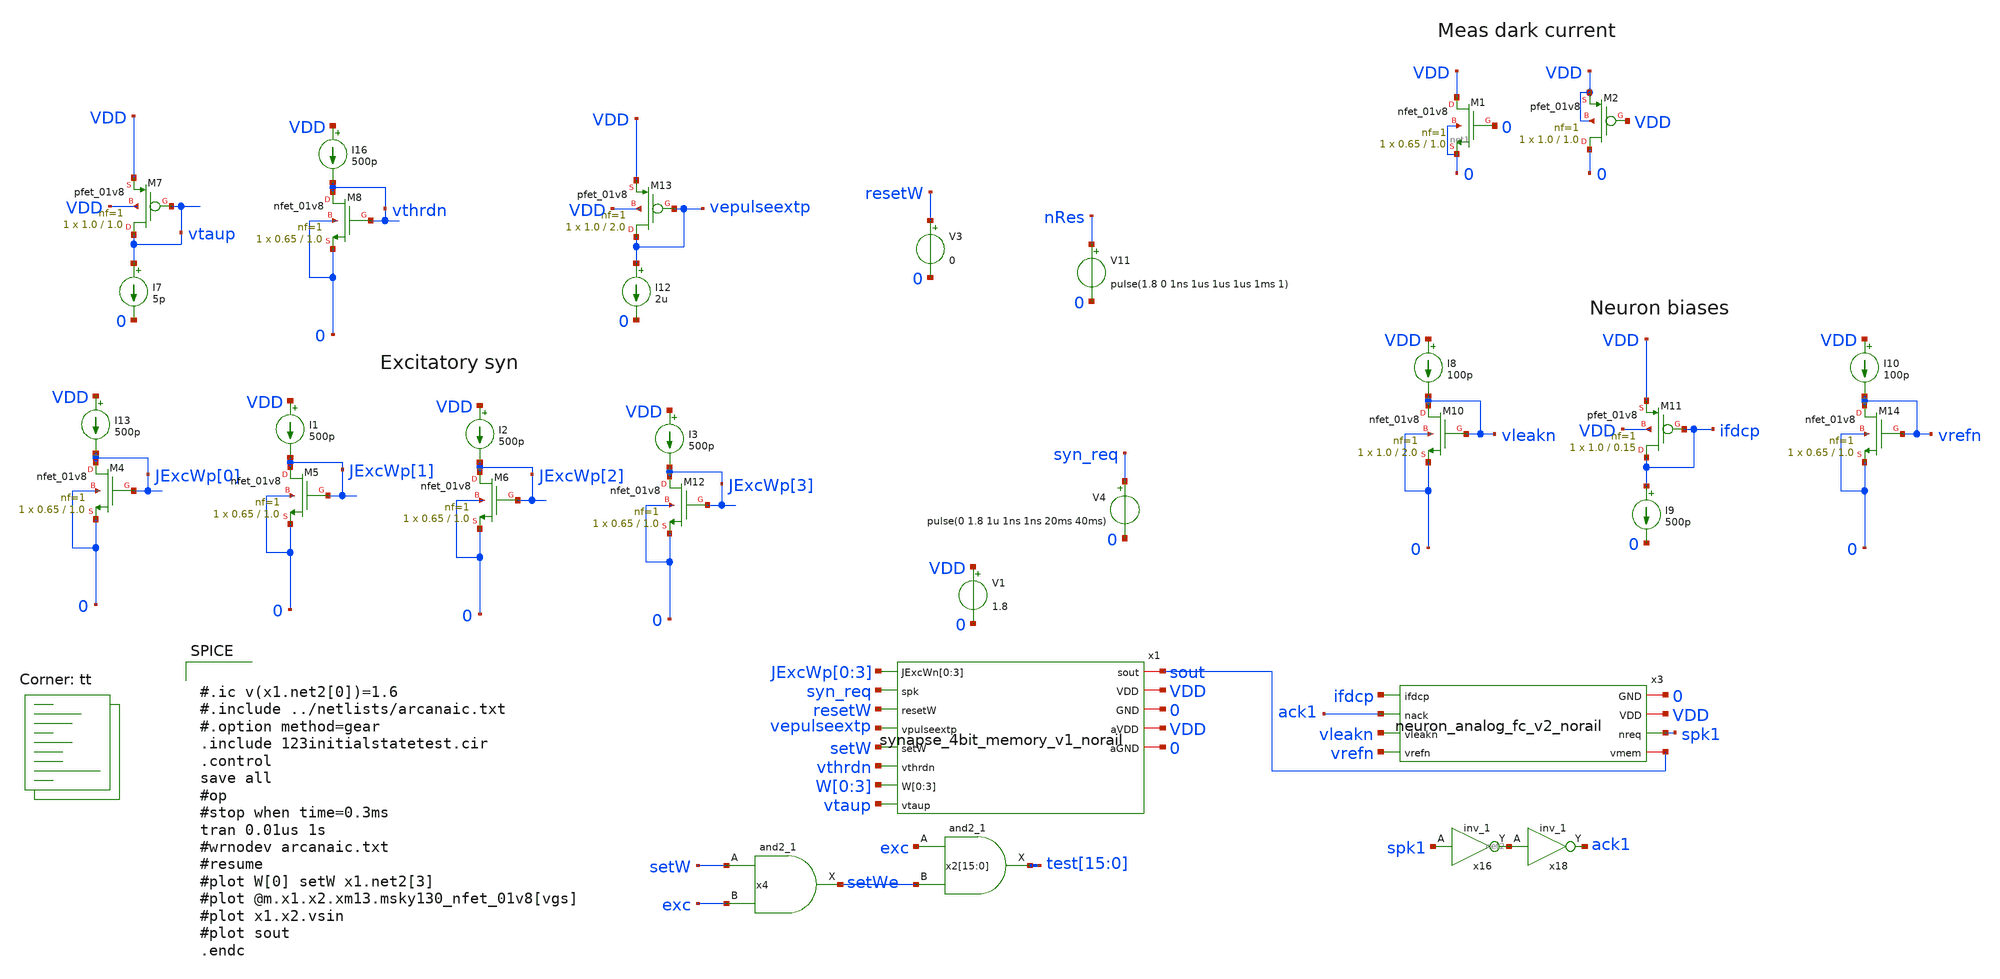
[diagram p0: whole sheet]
** sch_path: design/xschem/123initialstatetest.sch
**.subckt 123initialstatetest
x1 sout JExcWp[0] JExcWp[1] JExcWp[2] JExcWp[3] syn_req resetW vepulseextp setW vthrdn W[0] W[1]
+ W[2] W[3] vtaup VDD 0 VDD 0 synapse_4bit_memory_v1_norail
V1 VDD 0 1.8
XM7 vtaup vtaup VDD VDD sky130_fd_pr__pfet_01v8 L=1.0 W=1.0 nf=1 ad='int((nf+1)/2) * W/nf * 0.29' as='int((nf+2)/2) * W/nf * 0.29'
+ pd='2*int((nf+1)/2) * (W/nf + 0.29)' ps='2*int((nf+2)/2) * (W/nf + 0.29)' nrd='0.29 / W' nrs='0.29 / W'
+ sa=0 sb=0 sd=0 mult=1 m=1
I7 vtaup 0 5p
I16 VDD vthrdn 500p
XM8 vthrdn vthrdn 0 0 sky130_fd_pr__nfet_01v8 L=1.0 W=0.65 nf=1 ad='int((nf+1)/2) * W/nf * 0.29' as='int((nf+2)/2) * W/nf * 0.29'
+ pd='2*int((nf+1)/2) * (W/nf + 0.29)' ps='2*int((nf+2)/2) * (W/nf + 0.29)' nrd='0.29 / W' nrs='0.29 / W'
+ sa=0 sb=0 sd=0 mult=1 m=1
XM13 vepulseextp vepulseextp VDD VDD sky130_fd_pr__pfet_01v8 L=2.0 W=1.0 nf=1 ad='int((nf+1)/2) * W/nf * 0.29'
+ as='int((nf+2)/2) * W/nf * 0.29' pd='2*int((nf+1)/2) * (W/nf + 0.29)' ps='2*int((nf+2)/2) * (W/nf + 0.29)'
+ nrd='0.29 / W' nrs='0.29 / W' sa=0 sb=0 sd=0 mult=1 m=1
I12 vepulseextp 0 2u
V3 resetW 0 0
V11 nRes 0 pulse(1.8 0 1ns 1us 1us 1us 1ms 1)
x4 setW exc GND GND VDD VDD setWe sky130_fd_sc_hd__and2_1
x2[15] exc setWe GND GND VDD VDD test[15] sky130_fd_sc_hd__and2_1
x2[14] exc setWe GND GND VDD VDD test[14] sky130_fd_sc_hd__and2_1
x2[13] exc setWe GND GND VDD VDD test[13] sky130_fd_sc_hd__and2_1
x2[12] exc setWe GND GND VDD VDD test[12] sky130_fd_sc_hd__and2_1
x2[11] exc setWe GND GND VDD VDD test[11] sky130_fd_sc_hd__and2_1
x2[10] exc setWe GND GND VDD VDD test[10] sky130_fd_sc_hd__and2_1
x2[9] exc setWe GND GND VDD VDD test[9] sky130_fd_sc_hd__and2_1
x2[8] exc setWe GND GND VDD VDD test[8] sky130_fd_sc_hd__and2_1
x2[7] exc setWe GND GND VDD VDD test[7] sky130_fd_sc_hd__and2_1
x2[6] exc setWe GND GND VDD VDD test[6] sky130_fd_sc_hd__and2_1
x2[5] exc setWe GND GND VDD VDD test[5] sky130_fd_sc_hd__and2_1
x2[4] exc setWe GND GND VDD VDD test[4] sky130_fd_sc_hd__and2_1
x2[3] exc setWe GND GND VDD VDD test[3] sky130_fd_sc_hd__and2_1
x2[2] exc setWe GND GND VDD VDD test[2] sky130_fd_sc_hd__and2_1
x2[1] exc setWe GND GND VDD VDD test[1] sky130_fd_sc_hd__and2_1
x2[0] exc setWe GND GND VDD VDD test[0] sky130_fd_sc_hd__and2_1
V4 syn_req 0 pulse(0 1.8 1u 1ns 1ns 20ms 40ms)
XM1 VDD 0 0 net1 sky130_fd_pr__nfet_01v8 L=1.0 W=0.65 nf=1 ad='int((nf+1)/2) * W/nf * 0.29' as='int((nf+2)/2) * W/nf * 0.29'
+ pd='2*int((nf+1)/2) * (W/nf + 0.29)' ps='2*int((nf+2)/2) * (W/nf + 0.29)' nrd='0.29 / W' nrs='0.29 / W'
+ sa=0 sb=0 sd=0 mult=1 m=1
XM2 0 VDD VDD VDD sky130_fd_pr__pfet_01v8 L=1.0 W=1.0 nf=1 ad='int((nf+1)/2) * W/nf * 0.29' as='int((nf+2)/2) * W/nf * 0.29'
+ pd='2*int((nf+1)/2) * (W/nf + 0.29)' ps='2*int((nf+2)/2) * (W/nf + 0.29)' nrd='0.29 / W' nrs='0.29 / W'
+ sa=0 sb=0 sd=0 mult=1 m=1
x3 0 VDD spk1 ifdcp ack1 sout vleakn vrefn neuron_analog_fc_v2_norail
x16 spk1 0 0 VDD VDD net2 sky130_fd_sc_hd__inv_1
x18 net2 0 0 VDD VDD ack1 sky130_fd_sc_hd__inv_1
I8 VDD vleakn 100p
XM10 vleakn vleakn 0 0 sky130_fd_pr__nfet_01v8 L=2.0 W=1.0 nf=1 ad='int((nf+1)/2) * W/nf * 0.29' as='int((nf+2)/2) * W/nf * 0.29'
+ pd='2*int((nf+1)/2) * (W/nf + 0.29)' ps='2*int((nf+2)/2) * (W/nf + 0.29)' nrd='0.29 / W' nrs='0.29 / W'
+ sa=0 sb=0 sd=0 mult=1 m=1
XM11 ifdcp ifdcp VDD VDD sky130_fd_pr__pfet_01v8 L=0.15 W=1.0 nf=1 ad='int((nf+1)/2) * W/nf * 0.29' as='int((nf+2)/2) * W/nf * 0.29'
+ pd='2*int((nf+1)/2) * (W/nf + 0.29)' ps='2*int((nf+2)/2) * (W/nf + 0.29)' nrd='0.29 / W' nrs='0.29 / W'
+ sa=0 sb=0 sd=0 mult=1 m=1
I9 ifdcp 0 500p
I10 VDD vrefn 100p
XM14 vrefn vrefn 0 0 sky130_fd_pr__nfet_01v8 L=1.0 W=0.65 nf=1 ad='int((nf+1)/2) * W/nf * 0.29' as='int((nf+2)/2) * W/nf * 0.29'
+ pd='2*int((nf+1)/2) * (W/nf + 0.29)' ps='2*int((nf+2)/2) * (W/nf + 0.29)' nrd='0.29 / W' nrs='0.29 / W'
+ sa=0 sb=0 sd=0 mult=1 m=1
I13 VDD JExcWp[0] 500p
XM4 JExcWp[0] JExcWp[0] 0 0 sky130_fd_pr__nfet_01v8 L=1.0 W=0.65 nf=1 ad='int((nf+1)/2) * W/nf * 0.29'
+ as='int((nf+2)/2) * W/nf * 0.29' pd='2*int((nf+1)/2) * (W/nf + 0.29)' ps='2*int((nf+2)/2) * (W/nf + 0.29)'
+ nrd='0.29 / W' nrs='0.29 / W' sa=0 sb=0 sd=0 mult=1 m=1
I1 VDD JExcWp[1] 500p
XM5 JExcWp[1] JExcWp[1] 0 0 sky130_fd_pr__nfet_01v8 L=1.0 W=0.65 nf=1 ad='int((nf+1)/2) * W/nf * 0.29'
+ as='int((nf+2)/2) * W/nf * 0.29' pd='2*int((nf+1)/2) * (W/nf + 0.29)' ps='2*int((nf+2)/2) * (W/nf + 0.29)'
+ nrd='0.29 / W' nrs='0.29 / W' sa=0 sb=0 sd=0 mult=1 m=1
I2 VDD JExcWp[2] 500p
XM6 JExcWp[2] JExcWp[2] 0 0 sky130_fd_pr__nfet_01v8 L=1.0 W=0.65 nf=1 ad='int((nf+1)/2) * W/nf * 0.29'
+ as='int((nf+2)/2) * W/nf * 0.29' pd='2*int((nf+1)/2) * (W/nf + 0.29)' ps='2*int((nf+2)/2) * (W/nf + 0.29)'
+ nrd='0.29 / W' nrs='0.29 / W' sa=0 sb=0 sd=0 mult=1 m=1
I3 VDD JExcWp[3] 500p
XM12 JExcWp[3] JExcWp[3] 0 0 sky130_fd_pr__nfet_01v8 L=1.0 W=0.65 nf=1 ad='int((nf+1)/2) * W/nf * 0.29'
+ as='int((nf+2)/2) * W/nf * 0.29' pd='2*int((nf+1)/2) * (W/nf + 0.29)' ps='2*int((nf+2)/2) * (W/nf + 0.29)'
+ nrd='0.29 / W' nrs='0.29 / W' sa=0 sb=0 sd=0 mult=1 m=1
**** begin user architecture code
.lib $::SKYWATER_MODELS/sky130.lib.spice tt


#.ic v(x1.net2[0])=1.6
#.include ../netlists/arcanaic.txt
#.option method=gear
.include 123initialstatetest.cir
.control
save all
#op
#stop when time=0.3ms
tran 0.01us 1s
#wrnodev arcanaic.txt
#resume
#plot W[0] setW x1.net2[3]
#plot @m.x1.x2.xm13.msky130_nfet_01v8[vgs]
#plot x1.x2.vsin
#plot sout
.endc




* Standard cell simulation files
.include $::SKYWATER_STDCELLS/sky130_fd_sc_hd.spice


**** end user architecture code
**.ends

* expanding   symbol:  synapse_4bit_memory_v1_norail.sym # of pins=13
** sym_path: design/xschem/synapse_4bit_memory_v1_norail.sym
** sch_path: design/xschem/synapse_4bit_memory_v1_norail.sch
.subckt synapse_4bit_memory_v1_norail sout JExcWn[0] JExcWn[1] JExcWn[2] JExcWn[3] spk resetW
+ vpulseextp setW vthrdn W[0] W[1] W[2] W[3] vtaup VDD GND aVDD aGND
*.iopin GND
*.iopin VDD
*.ipin vpulseextp
*.ipin spk
*.ipin setW
*.ipin resetW
*.iopin sout
*.ipin vthrdn
*.ipin vtaup
*.iopin aVDD
*.ipin JExcWn[0],JExcWn[1],JExcWn[2],JExcWn[3]
*.ipin W[0],W[1],W[2],W[3]
*.iopin aGND
x2[0] setW W[0] net1 GND GND VDD VDD net2[3] sky130_fd_sc_hd__dfrtp_1
x2[1] setW W[1] net1 GND GND VDD VDD net2[2] sky130_fd_sc_hd__dfrtp_1
x2[2] setW W[2] net1 GND GND VDD VDD net2[1] sky130_fd_sc_hd__dfrtp_1
x2[3] setW W[3] net1 GND GND VDD VDD net2[0] sky130_fd_sc_hd__dfrtp_1
x4 resetW GND GND VDD VDD net1 sky130_fd_sc_hd__inv_1
x2 vtaup sout vthrdn spke JExcWn[0] JExcWn[1] JExcWn[2] JExcWn[3] aGND aVDD net2[3] net2[2] net2[1]
+ net2[0] dpi_syn_exc_4bit_fc_v2
x6 vpulseextp spk GND spke VDD spike_extender_with_trimming
x1 GND GND VDD VDD sky130_fd_sc_hd__decap_4
x3 GND GND VDD VDD sky130_fd_sc_hd__decap_3
x5 GND GND VDD VDD sky130_fd_sc_hd__decap_3
x7 GND GND VDD VDD sky130_fd_sc_hd__decap_6
x8 GND GND VDD VDD sky130_fd_sc_hd__decap_3
x9 GND GND VDD VDD sky130_fd_sc_hd__decap_3
.ends


* expanding   symbol:  neuron_analog_fc_v2_norail.sym # of pins=8
** sym_path: design/xschem/neuron_analog_fc_v2_norail.sym
** sch_path: design/xschem/neuron_analog_fc_v2_norail.sch
.subckt neuron_analog_fc_v2_norail GND VDD nreq ifdcp nack vmem vleakn vrefn
*.ipin vleakn
*.iopin GND
*.iopin VDD
*.opin nreq
*.ipin vrefn
*.ipin nack
*.ipin ifdcp
*.iopin vmem
XC1 GND vmem sky130_fd_pr__cap_mim_m3_1 W=5 L=5 MF=1 m=1
XM1 vmem ifdcp VDD VDD sky130_fd_pr__pfet_01v8 L=2.0 W=1.0 nf=1 ad='int((nf+1)/2) * W/nf * 0.29' as='int((nf+2)/2) * W/nf * 0.29'
+ pd='2*int((nf+1)/2) * (W/nf + 0.29)' ps='2*int((nf+2)/2) * (W/nf + 0.29)' nrd='0.29 / W' nrs='0.29 / W'
+ sa=0 sb=0 sd=0 mult=1 m=1
XM5 net2 nreq VDD VDD sky130_fd_pr__pfet_01v8 L=0.25 W=1.0 nf=1 ad='int((nf+1)/2) * W/nf * 0.29' as='int((nf+2)/2) * W/nf * 0.29'
+ pd='2*int((nf+1)/2) * (W/nf + 0.29)' ps='2*int((nf+2)/2) * (W/nf + 0.29)' nrd='0.29 / W' nrs='0.29 / W'
+ sa=0 sb=0 sd=0 mult=1 m=1
XM7 net3 nreq net4 GND sky130_fd_pr__nfet_01v8 L=0.15 W=0.6 nf=1 ad='int((nf+1)/2) * W/nf * 0.29' as='int((nf+2)/2) * W/nf * 0.29'
+ pd='2*int((nf+1)/2) * (W/nf + 0.29)' ps='2*int((nf+2)/2) * (W/nf + 0.29)' nrd='0.29 / W' nrs='0.29 / W'
+ sa=0 sb=0 sd=0 mult=1 m=1
XM6 net5 nack VDD VDD sky130_fd_pr__pfet_01v8 L=0.25 W=1.0 nf=1 ad='int((nf+1)/2) * W/nf * 0.29' as='int((nf+2)/2) * W/nf * 0.29'
+ pd='2*int((nf+1)/2) * (W/nf + 0.29)' ps='2*int((nf+2)/2) * (W/nf + 0.29)' nrd='0.29 / W' nrs='0.29 / W'
+ sa=0 sb=0 sd=0 mult=1 m=1
XM9 nreq vmem net2 VDD sky130_fd_pr__pfet_01v8 L=0.15 W=1.0 nf=1 ad='int((nf+1)/2) * W/nf * 0.29' as='int((nf+2)/2) * W/nf * 0.29'
+ pd='2*int((nf+1)/2) * (W/nf + 0.29)' ps='2*int((nf+2)/2) * (W/nf + 0.29)' nrd='0.29 / W' nrs='0.29 / W'
+ sa=0 sb=0 sd=0 mult=1 m=1
XM10 net3 nreq net5 VDD sky130_fd_pr__pfet_01v8 L=0.15 W=1.0 nf=1 ad='int((nf+1)/2) * W/nf * 0.29' as='int((nf+2)/2) * W/nf * 0.29'
+ pd='2*int((nf+1)/2) * (W/nf + 0.29)' ps='2*int((nf+2)/2) * (W/nf + 0.29)' nrd='0.29 / W' nrs='0.29 / W'
+ sa=0 sb=0 sd=0 mult=1 m=1
XM4 vmem nreq VDD VDD sky130_fd_pr__pfet_01v8 L=1.0 W=1.0 nf=1 ad='int((nf+1)/2) * W/nf * 0.29' as='int((nf+2)/2) * W/nf * 0.29'
+ pd='2*int((nf+1)/2) * (W/nf + 0.29)' ps='2*int((nf+2)/2) * (W/nf + 0.29)' nrd='0.29 / W' nrs='0.29 / W'
+ sa=0 sb=0 sd=0 mult=1 m=1
XM2 nreq vmem net1 GND sky130_fd_pr__nfet_01v8 L=0.15 W=0.6 nf=1 ad='int((nf+1)/2) * W/nf * 0.29' as='int((nf+2)/2) * W/nf * 0.29'
+ pd='2*int((nf+1)/2) * (W/nf + 0.29)' ps='2*int((nf+2)/2) * (W/nf + 0.29)' nrd='0.29 / W' nrs='0.29 / W'
+ sa=0 sb=0 sd=0 mult=1 m=1
XM3 net4 vrefn GND GND sky130_fd_pr__nfet_01v8 L=1.0 W=0.6 nf=1 ad='int((nf+1)/2) * W/nf * 0.29' as='int((nf+2)/2) * W/nf * 0.29'
+ pd='2*int((nf+1)/2) * (W/nf + 0.29)' ps='2*int((nf+2)/2) * (W/nf + 0.29)' nrd='0.29 / W' nrs='0.29 / W'
+ sa=0 sb=0 sd=0 mult=1 m=1
XM8 net1 net1 GND GND sky130_fd_pr__nfet_01v8 L=0.15 W=0.6 nf=1 ad='int((nf+1)/2) * W/nf * 0.29' as='int((nf+2)/2) * W/nf * 0.29'
+ pd='2*int((nf+1)/2) * (W/nf + 0.29)' ps='2*int((nf+2)/2) * (W/nf + 0.29)' nrd='0.29 / W' nrs='0.29 / W'
+ sa=0 sb=0 sd=0 mult=1 m=1
XM11 vmem net3 GND GND sky130_fd_pr__nfet_01v8 L=0.2 W=1.0 nf=1 ad='int((nf+1)/2) * W/nf * 0.29' as='int((nf+2)/2) * W/nf * 0.29'
+ pd='2*int((nf+1)/2) * (W/nf + 0.29)' ps='2*int((nf+2)/2) * (W/nf + 0.29)' nrd='0.29 / W' nrs='0.29 / W'
+ sa=0 sb=0 sd=0 mult=1 m=1
XM12 vmem vleakn GND GND sky130_fd_pr__nfet_01v8 L=2.0 W=1.0 nf=1 ad='int((nf+1)/2) * W/nf * 0.29' as='int((nf+2)/2) * W/nf * 0.29'
+ pd='2*int((nf+1)/2) * (W/nf + 0.29)' ps='2*int((nf+2)/2) * (W/nf + 0.29)' nrd='0.29 / W' nrs='0.29 / W'
+ sa=0 sb=0 sd=0 mult=1 m=1
XM13 GND net3 GND GND sky130_fd_pr__nfet_01v8 L=2.0 W=1.0 nf=1 ad='int((nf+1)/2) * W/nf * 0.29' as='int((nf+2)/2) * W/nf * 0.29'
+ pd='2*int((nf+1)/2) * (W/nf + 0.29)' ps='2*int((nf+2)/2) * (W/nf + 0.29)' nrd='0.29 / W' nrs='0.29 / W'
+ sa=0 sb=0 sd=0 mult=1 m=1
.ends


* expanding   symbol:  dpi_syn_exc_4bit_fc_v2.sym # of pins=8
** sym_path: design/xschem/dpi_syn_exc_4bit_fc_v2.sym
** sch_path: design/xschem/dpi_syn_exc_4bit_fc_v2.sch
.subckt dpi_syn_exc_4bit_fc_v2 vtaup sout vthn spk JExcWn[0] JExcWn[1] JExcWn[2] JExcWn[3] GND aVDD
+ weight[0] weight[1] weight[2] weight[3]
*.iopin GND
*.iopin aVDD
*.iopin vtaup
*.ipin spk
*.opin sout
*.iopin vthn
*.ipin weight[0],weight[1],weight[2],weight[3]
*.iopin JExcWn[0],JExcWn[1],JExcWn[2],JExcWn[3]
XM2 net3 spk net1 GND sky130_fd_pr__nfet_01v8 L=0.25 W=1.0 nf=1 ad='int((nf+1)/2) * W/nf * 0.29' as='int((nf+2)/2) * W/nf * 0.29'
+ pd='2*int((nf+1)/2) * (W/nf + 0.29)' ps='2*int((nf+2)/2) * (W/nf + 0.29)' nrd='0.29 / W' nrs='0.29 / W'
+ sa=0 sb=0 sd=0 mult=1 m=1
XC1 vsin aVDD sky130_fd_pr__cap_mim_m3_1 W=5 L=5 MF=1 m=1
XM5 vsin vtaup aVDD aVDD sky130_fd_pr__pfet_01v8 L=0.2 W=1.2 nf=1 ad='int((nf+1)/2) * W/nf * 0.29' as='int((nf+2)/2) * W/nf * 0.29'
+ pd='2*int((nf+1)/2) * (W/nf + 0.29)' ps='2*int((nf+2)/2) * (W/nf + 0.29)' nrd='0.29 / W' nrs='0.29 / W'
+ sa=0 sb=0 sd=0 mult=1 m=1
XM6 sout vsin aVDD aVDD sky130_fd_pr__pfet_01v8 L=0.2 W=1.2 nf=1 ad='int((nf+1)/2) * W/nf * 0.29' as='int((nf+2)/2) * W/nf * 0.29'
+ pd='2*int((nf+1)/2) * (W/nf + 0.29)' ps='2*int((nf+2)/2) * (W/nf + 0.29)' nrd='0.29 / W' nrs='0.29 / W'
+ sa=0 sb=0 sd=0 mult=1 m=1
XM1 net1 JExcWn[0] net2 GND sky130_fd_pr__nfet_01v8 L=1.0 W=1.0 nf=1 ad='int((nf+1)/2) * W/nf * 0.29'
+ as='int((nf+2)/2) * W/nf * 0.29' pd='2*int((nf+1)/2) * (W/nf + 0.29)' ps='2*int((nf+2)/2) * (W/nf + 0.29)'
+ nrd='0.29 / W' nrs='0.29 / W' sa=0 sb=0 sd=0 mult=1 m=1
XM4 vsin vsin net3 GND sky130_fd_pr__nfet_01v8 L=0.25 W=1.0 nf=1 ad='int((nf+1)/2) * W/nf * 0.29' as='int((nf+2)/2) * W/nf * 0.29'
+ pd='2*int((nf+1)/2) * (W/nf + 0.29)' ps='2*int((nf+2)/2) * (W/nf + 0.29)' nrd='0.29 / W' nrs='0.29 / W'
+ sa=0 sb=0 sd=0 mult=1 m=1
XM3 aVDD vthn net3 GND sky130_fd_pr__nfet_01v8 L=0.25 W=1.0 nf=1 ad='int((nf+1)/2) * W/nf * 0.29' as='int((nf+2)/2) * W/nf * 0.29'
+ pd='2*int((nf+1)/2) * (W/nf + 0.29)' ps='2*int((nf+2)/2) * (W/nf + 0.29)' nrd='0.29 / W' nrs='0.29 / W'
+ sa=0 sb=0 sd=0 mult=1 m=1
XM7 net1 JExcWn[1] net4 GND sky130_fd_pr__nfet_01v8 L=2.0 W=1.0 nf=1 ad='int((nf+1)/2) * W/nf * 0.29'
+ as='int((nf+2)/2) * W/nf * 0.29' pd='2*int((nf+1)/2) * (W/nf + 0.29)' ps='2*int((nf+2)/2) * (W/nf + 0.29)'
+ nrd='0.29 / W' nrs='0.29 / W' sa=0 sb=0 sd=0 mult=1 m=1
XM8 net1 JExcWn[2] net5 GND sky130_fd_pr__nfet_01v8 L=4.0 W=1.0 nf=1 ad='int((nf+1)/2) * W/nf * 0.29'
+ as='int((nf+2)/2) * W/nf * 0.29' pd='2*int((nf+1)/2) * (W/nf + 0.29)' ps='2*int((nf+2)/2) * (W/nf + 0.29)'
+ nrd='0.29 / W' nrs='0.29 / W' sa=0 sb=0 sd=0 mult=1 m=1
XM9 net1 JExcWn[3] net6 GND sky130_fd_pr__nfet_01v8 L=8.0 W=1.0 nf=1 ad='int((nf+1)/2) * W/nf * 0.29'
+ as='int((nf+2)/2) * W/nf * 0.29' pd='2*int((nf+1)/2) * (W/nf + 0.29)' ps='2*int((nf+2)/2) * (W/nf + 0.29)'
+ nrd='0.29 / W' nrs='0.29 / W' sa=0 sb=0 sd=0 mult=1 m=1
XM10 net2 weight[0] GND GND sky130_fd_pr__nfet_01v8 L=0.25 W=1.0 nf=1 ad='int((nf+1)/2) * W/nf * 0.29'
+ as='int((nf+2)/2) * W/nf * 0.29' pd='2*int((nf+1)/2) * (W/nf + 0.29)' ps='2*int((nf+2)/2) * (W/nf + 0.29)'
+ nrd='0.29 / W' nrs='0.29 / W' sa=0 sb=0 sd=0 mult=1 m=1
XM11 net4 weight[1] GND GND sky130_fd_pr__nfet_01v8 L=0.25 W=1.0 nf=1 ad='int((nf+1)/2) * W/nf * 0.29'
+ as='int((nf+2)/2) * W/nf * 0.29' pd='2*int((nf+1)/2) * (W/nf + 0.29)' ps='2*int((nf+2)/2) * (W/nf + 0.29)'
+ nrd='0.29 / W' nrs='0.29 / W' sa=0 sb=0 sd=0 mult=1 m=1
XM12 net5 weight[2] GND GND sky130_fd_pr__nfet_01v8 L=0.25 W=1.0 nf=1 ad='int((nf+1)/2) * W/nf * 0.29'
+ as='int((nf+2)/2) * W/nf * 0.29' pd='2*int((nf+1)/2) * (W/nf + 0.29)' ps='2*int((nf+2)/2) * (W/nf + 0.29)'
+ nrd='0.29 / W' nrs='0.29 / W' sa=0 sb=0 sd=0 mult=1 m=1
XM13 net6 weight[3] GND GND sky130_fd_pr__nfet_01v8 L=0.25 W=1.0 nf=1 ad='int((nf+1)/2) * W/nf * 0.29'
+ as='int((nf+2)/2) * W/nf * 0.29' pd='2*int((nf+1)/2) * (W/nf + 0.29)' ps='2*int((nf+2)/2) * (W/nf + 0.29)'
+ nrd='0.29 / W' nrs='0.29 / W' sa=0 sb=0 sd=0 mult=1 m=1
.ends


* expanding   symbol:  spike_extender_with_trimming.sym # of pins=5
** sym_path: design/xschem/spike_extender_with_trimming.sym
** sch_path: design/xschem/spike_extender_with_trimming.sch
.subckt spike_extender_with_trimming vpulseextp vspk GND spkext VDD
*.iopin GND
*.iopin VDD
*.ipin vspk
*.opin spkext
*.ipin vpulseextp
x1 vpulseextp vpulseshort GND spkext VDD spike_extender
x3 vspk GND GND VDD VDD net1 sky130_fd_sc_hd__clkdlybuf4s50_1
x2 net1 vspk GND GND VDD VDD vpulseshort sky130_fd_sc_hd__nor2b_1
.ends


* expanding   symbol:  spike_extender.sym # of pins=5
** sym_path: design/xschem/spike_extender.sym
** sch_path: design/xschem/spike_extender.sch
.subckt spike_extender vpulseextp spk GND spkext VDD
*.iopin GND
*.iopin VDD
*.ipin spk
*.opin spkext
*.ipin vpulseextp
XM1 net1 spk GND GND sky130_fd_pr__nfet_01v8 L=0.15 W=0.65 nf=1 ad='int((nf+1)/2) * W/nf * 0.29' as='int((nf+2)/2) * W/nf * 0.29'
+ pd='2*int((nf+1)/2) * (W/nf + 0.29)' ps='2*int((nf+2)/2) * (W/nf + 0.29)' nrd='0.29 / W' nrs='0.29 / W'
+ sa=0 sb=0 sd=0 mult=1 m=1
XM6 net1 vpulseextp VDD VDD sky130_fd_pr__pfet_01v8 L=2 W=1 nf=1 ad='int((nf+1)/2) * W/nf * 0.29' as='int((nf+2)/2) * W/nf * 0.29'
+ pd='2*int((nf+1)/2) * (W/nf + 0.29)' ps='2*int((nf+2)/2) * (W/nf + 0.29)' nrd='0.29 / W' nrs='0.29 / W'
+ sa=0 sb=0 sd=0 mult=1 m=1
XM5 net3 net2 GND GND sky130_fd_pr__nfet_01v8 L=0.15 W=0.65 nf=1 ad='int((nf+1)/2) * W/nf * 0.29' as='int((nf+2)/2) * W/nf * 0.29'
+ pd='2*int((nf+1)/2) * (W/nf + 0.29)' ps='2*int((nf+2)/2) * (W/nf + 0.29)' nrd='0.29 / W' nrs='0.29 / W'
+ sa=0 sb=0 sd=0 mult=1 m=1
XM8 spkext net3 GND GND sky130_fd_pr__nfet_01v8 L=0.15 W=0.65 nf=1 ad='int((nf+1)/2) * W/nf * 0.29' as='int((nf+2)/2) * W/nf * 0.29'
+ pd='2*int((nf+1)/2) * (W/nf + 0.29)' ps='2*int((nf+2)/2) * (W/nf + 0.29)' nrd='0.29 / W' nrs='0.29 / W'
+ sa=0 sb=0 sd=0 mult=1 m=1
XM4 net3 net2 VDD VDD sky130_fd_pr__pfet_01v8 L=0.15 W=1.0 nf=1 ad='int((nf+1)/2) * W/nf * 0.29' as='int((nf+2)/2) * W/nf * 0.29'
+ pd='2*int((nf+1)/2) * (W/nf + 0.29)' ps='2*int((nf+2)/2) * (W/nf + 0.29)' nrd='0.29 / W' nrs='0.29 / W'
+ sa=0 sb=0 sd=0 mult=1 m=1
XM7 spkext net3 VDD VDD sky130_fd_pr__pfet_01v8 L=0.15 W=1.0 nf=1 ad='int((nf+1)/2) * W/nf * 0.29' as='int((nf+2)/2) * W/nf * 0.29'
+ pd='2*int((nf+1)/2) * (W/nf + 0.29)' ps='2*int((nf+2)/2) * (W/nf + 0.29)' nrd='0.29 / W' nrs='0.29 / W'
+ sa=0 sb=0 sd=0 mult=1 m=1
XM2 net2 net1 GND GND sky130_fd_pr__nfet_01v8 L=0.15 W=0.65 nf=1 ad='int((nf+1)/2) * W/nf * 0.29' as='int((nf+2)/2) * W/nf * 0.29'
+ pd='2*int((nf+1)/2) * (W/nf + 0.29)' ps='2*int((nf+2)/2) * (W/nf + 0.29)' nrd='0.29 / W' nrs='0.29 / W'
+ sa=0 sb=0 sd=0 mult=1 m=1
XM3 net2 net1 VDD VDD sky130_fd_pr__pfet_01v8 L=0.15 W=1.0 nf=1 ad='int((nf+1)/2) * W/nf * 0.29' as='int((nf+2)/2) * W/nf * 0.29'
+ pd='2*int((nf+1)/2) * (W/nf + 0.29)' ps='2*int((nf+2)/2) * (W/nf + 0.29)' nrd='0.29 / W' nrs='0.29 / W'
+ sa=0 sb=0 sd=0 mult=1 m=1
XM9 GND net1 GND GND sky130_fd_pr__nfet_01v8 L=1 W=0.65 nf=1 ad='int((nf+1)/2) * W/nf * 0.29' as='int((nf+2)/2) * W/nf * 0.29'
+ pd='2*int((nf+1)/2) * (W/nf + 0.29)' ps='2*int((nf+2)/2) * (W/nf + 0.29)' nrd='0.29 / W' nrs='0.29 / W'
+ sa=0 sb=0 sd=0 mult=1 m=1
.ends

.end
